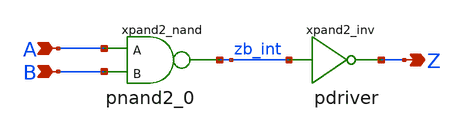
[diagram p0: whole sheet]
** sch_path: sram_2_16_scn4m/pand2.sch
**.subckt pand2 A B Z
*.ipin A
*.ipin B
*.opin Z
xpand2_nand A B zb_int vdd gnd pnand2_0
xpand2_inv zb_int Z vdd gnd pdriver
**** begin user architecture code


**** end user architecture code
**.ends

* expanding   symbol:  pnand2_0.sym # of pins=3
** sym_path: sram_2_16_scn4m/pnand2_0.sym
** sch_path: sram_2_16_scn4m/pnand2_0.sch
.subckt pnand2_0 A B Z vdd gnd
*.ipin A
*.ipin B
*.opin Z
*.iopin vdd
*.iopin gnd
Mpnand2_nmos1 Z B net1 gnd n w=1.6u l=0.4u m=1
Mpnand2_pmos1 Z A vdd vdd p w=1.6u l=0.4u m=1
Mpnand2_pmos2 Z B vdd vdd p w=1.6u l=0.4u m=1
Mpnand2_nmos2 net1 A gnd gnd n w=1.6u l=0.4u m=1
.ends


* expanding   symbol:  pdriver.sym # of pins=2
** sym_path: sram_4_16_scn4m/pdriver.sym
** sch_path: sram_4_16_scn4m/pdriver.sch
.subckt pdriver A Z vdd gnd
*.ipin A
*.opin Z
xbuf_inv1 A Z vdd gnd pinv_2
.ends


* expanding   symbol:  pinv_2.sym # of pins=2
** sym_path: sram_2_64_scn4m/pinv_2.sym
** sch_path: sram_2_64_scn4m/pinv_2.sch
.subckt pinv_2 A Z vdd gnd
*.ipin A
*.opin Z
Mpinv_nmos Z A gnd gnd n w=0.8u l=0.4u m=1
Mp_inv_pmos Z A vdd vdd p w=1.6u l=0.4u m=1
.ends

.end
